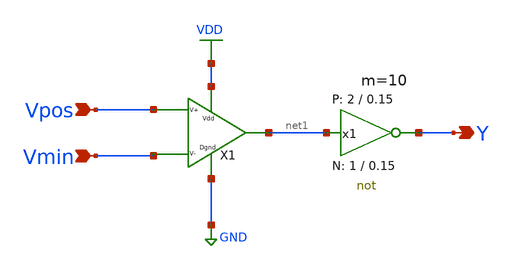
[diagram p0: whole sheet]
** sch_path: skywater_comparator.sch
* Copyright 2021 Stefan Frederik Schippers
* Licensed under the Apache License, Version 2.0 (the "License");
* you may not use this file except in compliance with the License.
* You may obtain a copy of the License at
* https://www.apache.org/licenses/LICENSE-2.0
* Unless required by applicable law or agreed to in writing, software
* distributed under the License is distributed on an "AS IS" BASIS,
* WITHOUT WARRANTIES OR CONDITIONS OF ANY KIND, either express or implied.
* See the License for the specific language governing permissions and
* limitations under the License.
**.subckt skywater_comparator Vpos Vmin Y
*.ipin Vpos
*.ipin Vmin
*.opin Y
X1 Vmin Vpos net1 VDD GND opamp_sky130
x1 Y net1 VDD GND not W_N=1 L_N=0.15 W_P=2 L_P=0.15 m=10
**.ends

* expanding   symbol:  sky130_tests/not.sym # of pins=2
** sym_path: sky130_tests/not.sym
** sch_path: sky130_tests/not.sch
.subckt not y a VCCPIN VSSPIN     W_N=1 L_N=0.15 W_P=2 L_P=0.15
*.opin y
*.ipin a
XM1 DN a VSSPIN VSSPIN sky130_fd_pr__nfet_01v8 L=L_N W=W_N nf=1 ad='int((1 + 1)/2) * W_N / 1 * 0.29'
+ as='int((1 + 2)/2) * W_N / 1 * 0.29' pd='2*int((1 + 1)/2) * (W_N / 1 + 0.29)' ps='2*int((1 + 2)/2) * (W_N / 1 + 0.29)'
+ nrd='0.29 / W_N ' nrs='0.29 / W_N ' sa=0 sb=0 sd=0 mult=1 m=1
XM2 DP a VCCPIN VCCPIN sky130_fd_pr__pfet_01v8 L=L_P W=W_P nf=1 ad='int((nf+1)/2) * W/nf * 0.29' as='int((nf+2)/2) * W/nf * 0.29'
+ pd='2*int((nf+1)/2) * (W/nf + 0.29)' ps='2*int((nf+2)/2) * (W/nf + 0.29)' nrd='0.29 / W' nrs='0.29 / W'
+ sa=0 sb=0 sd=0 mult=1 m=1
Vmeas DP y 0
.save i(vmeas)
Vmeas1 y DN 0
.save i(vmeas1)
.save v(dp)
.save v(dn)
.ends

.GLOBAL VDD
.GLOBAL GND
.end
